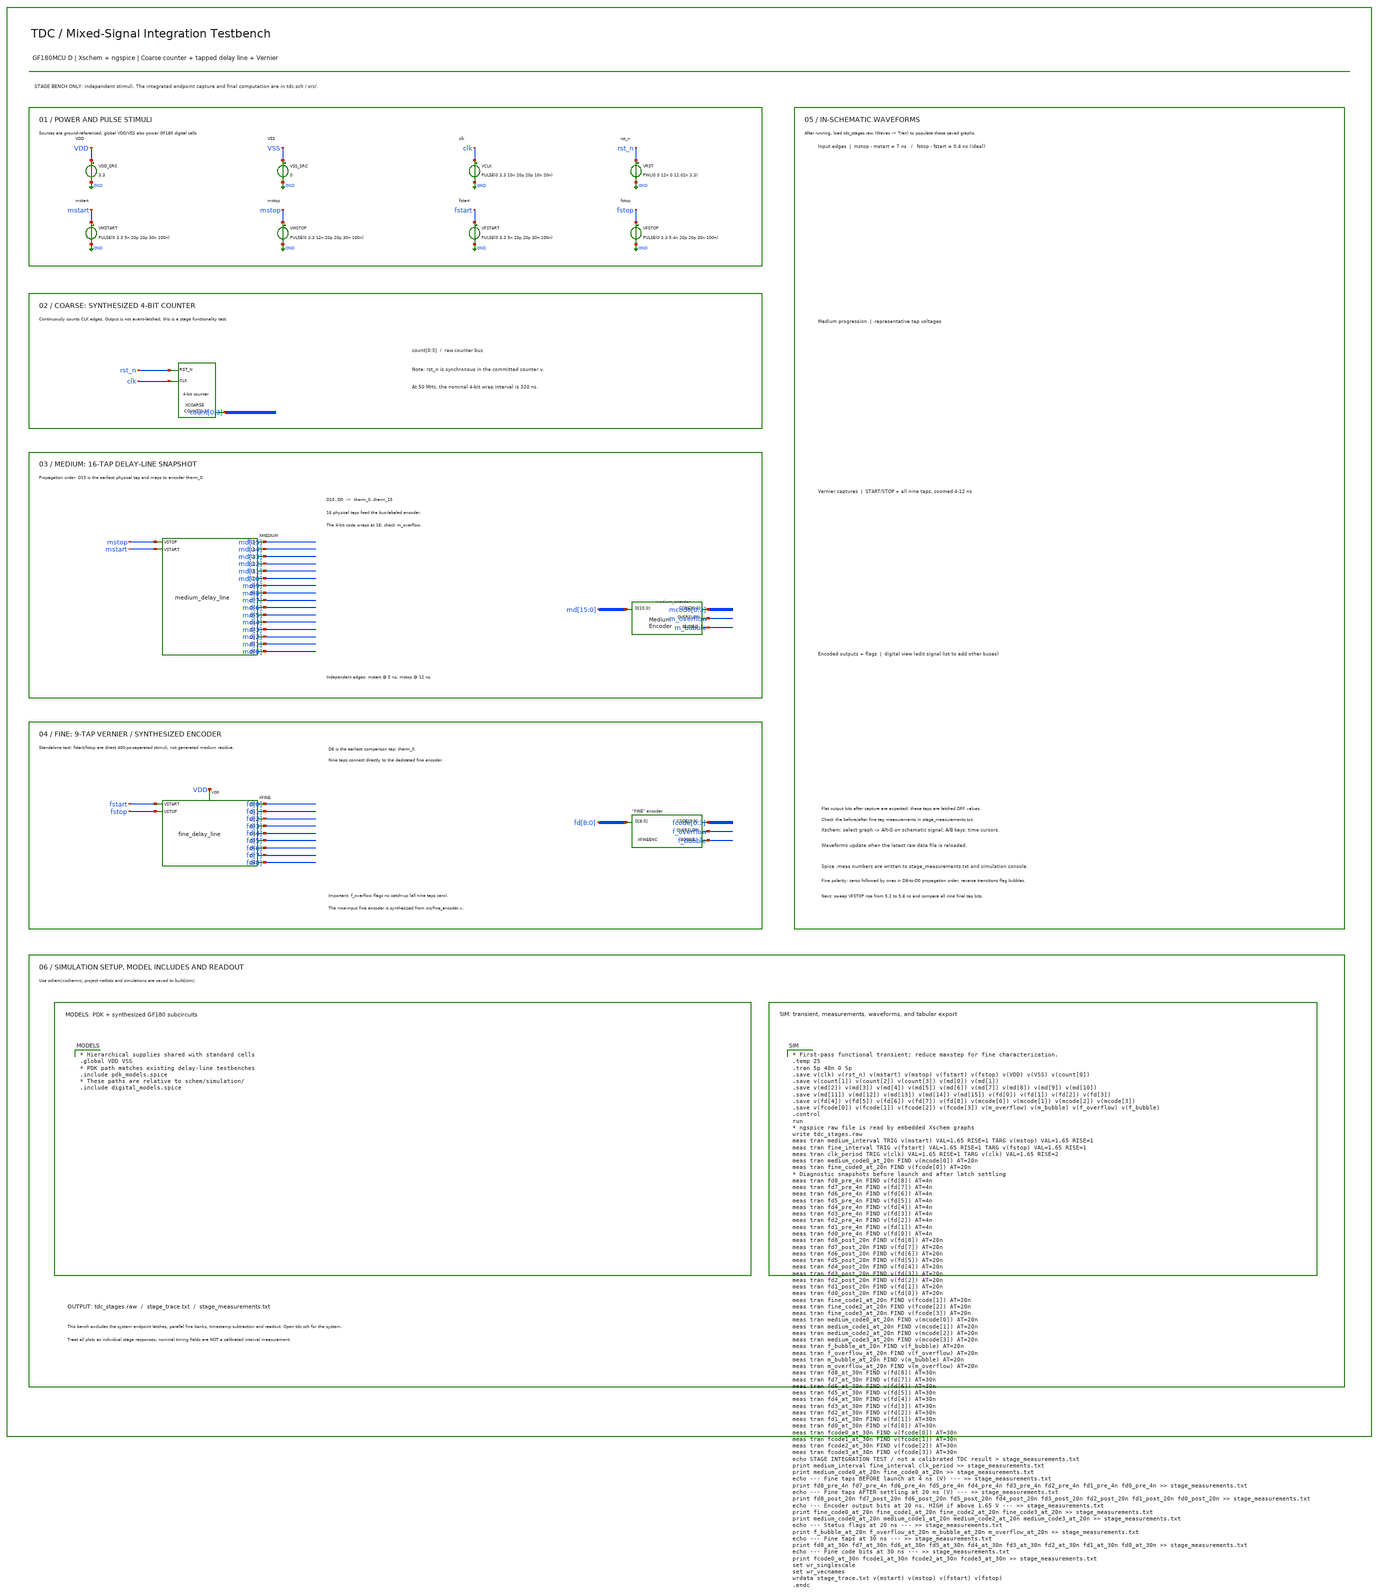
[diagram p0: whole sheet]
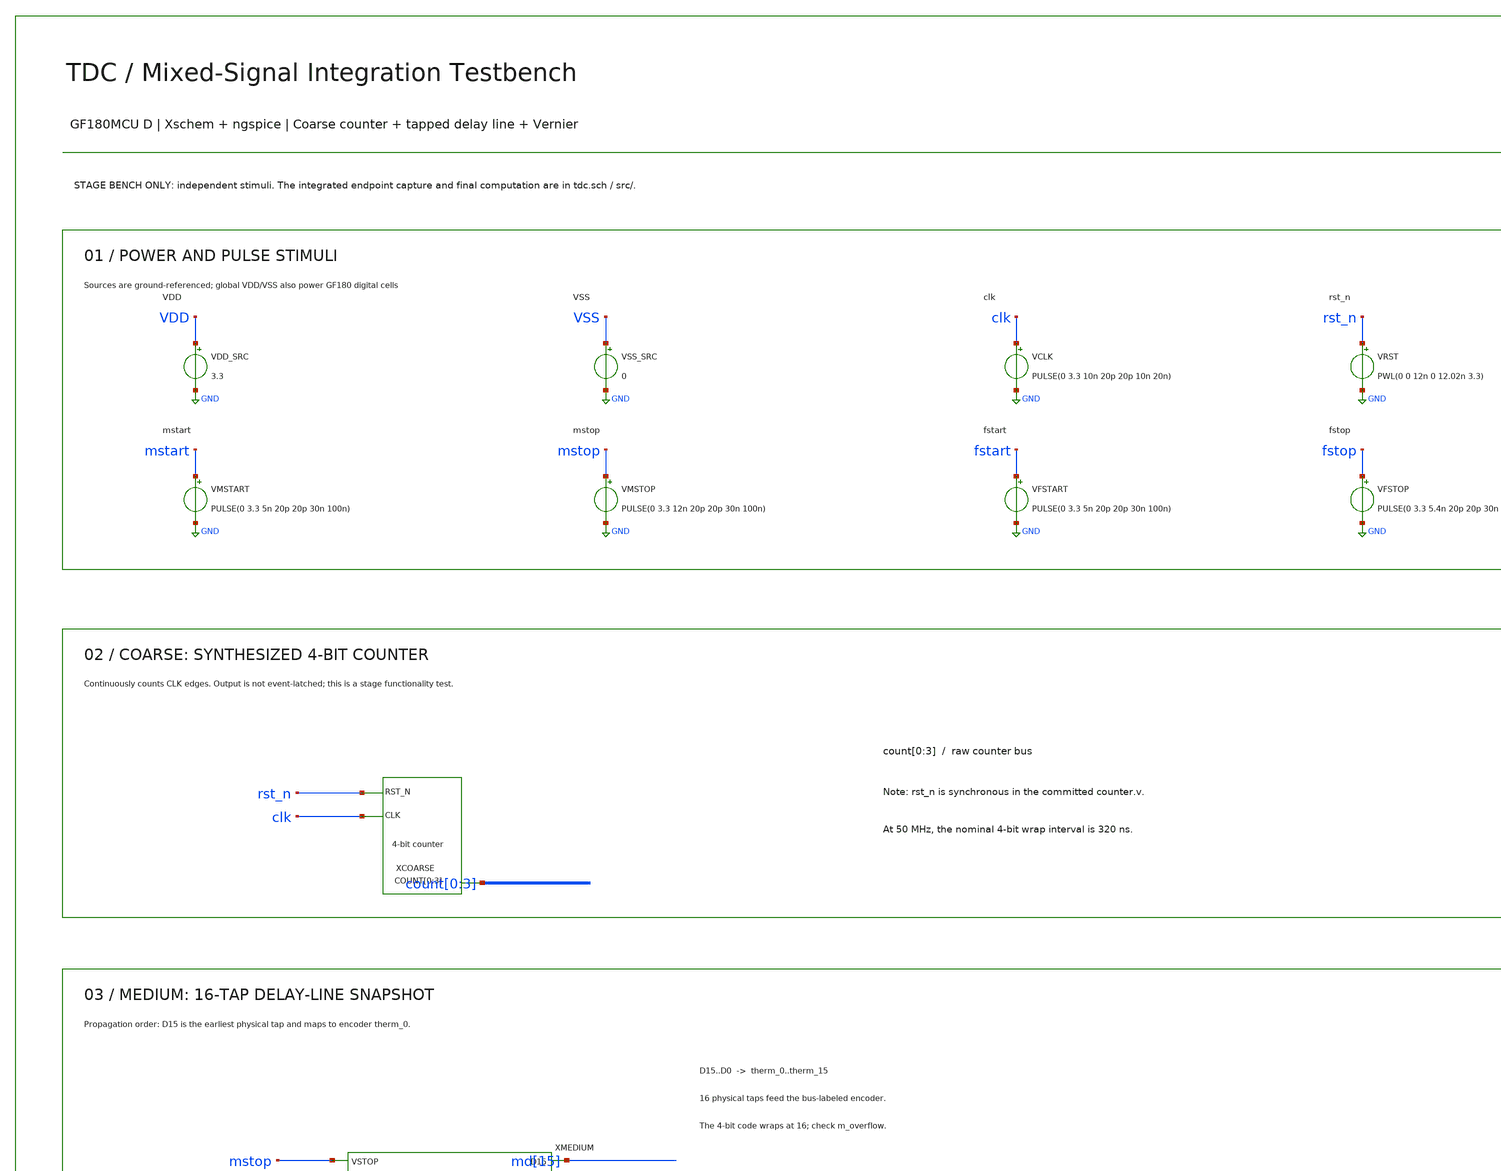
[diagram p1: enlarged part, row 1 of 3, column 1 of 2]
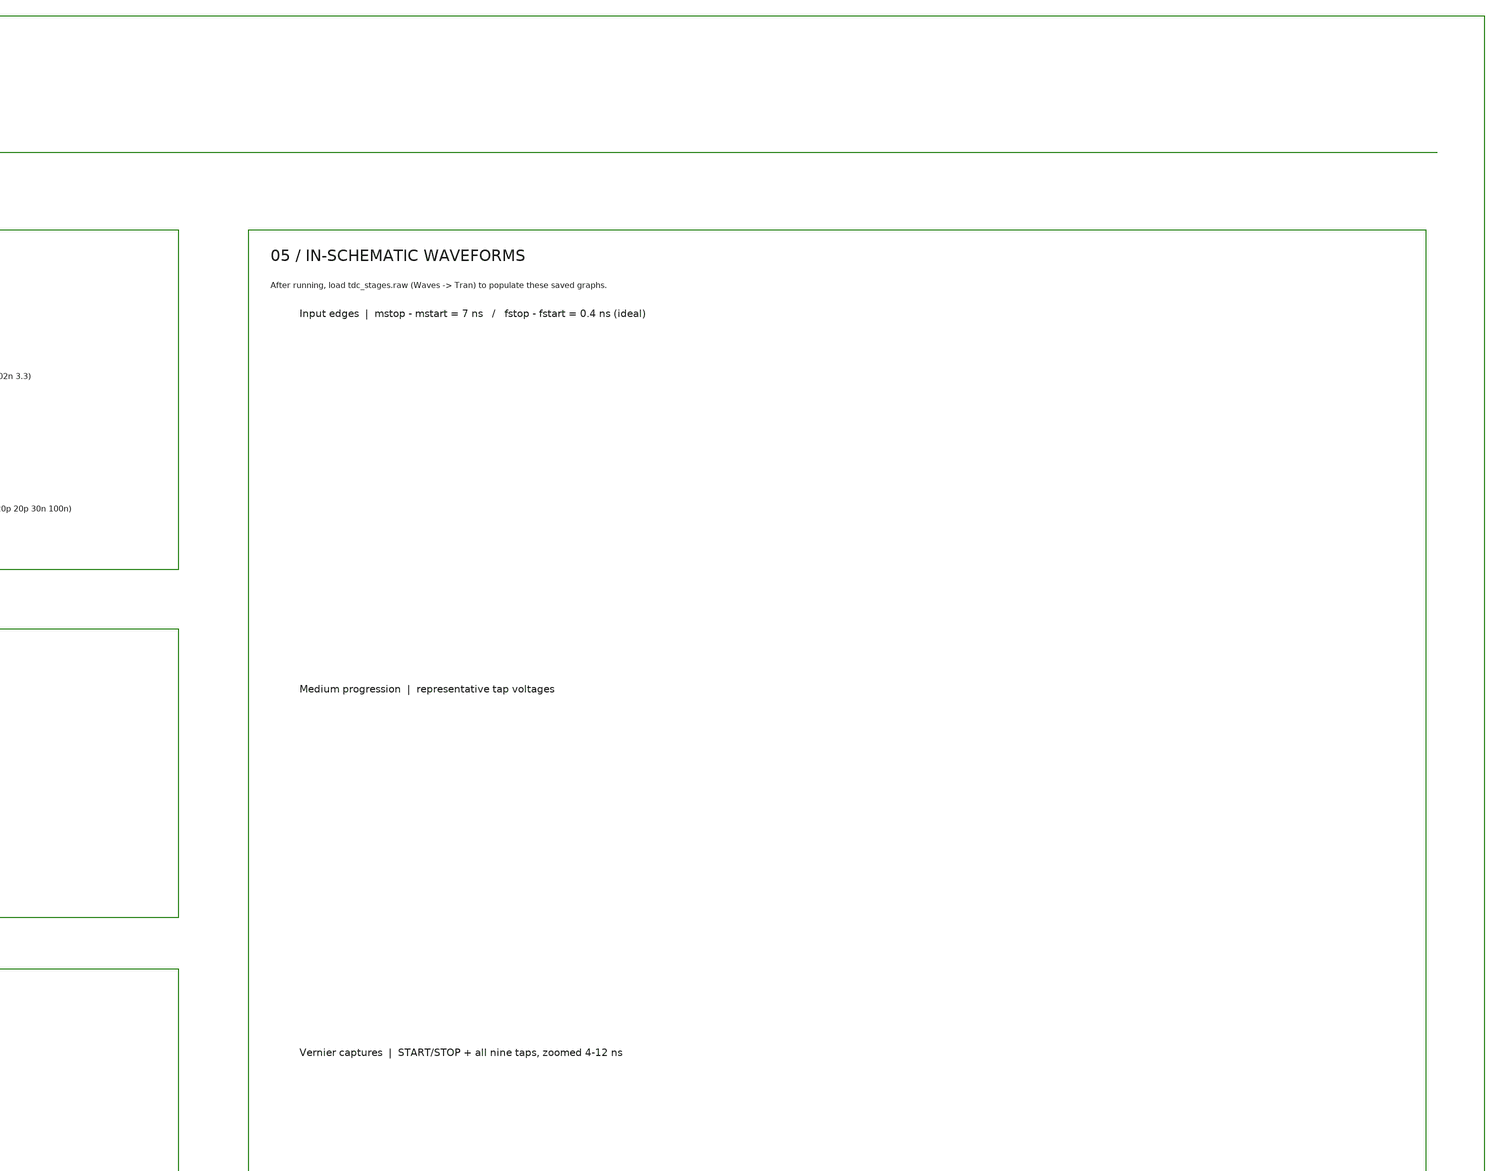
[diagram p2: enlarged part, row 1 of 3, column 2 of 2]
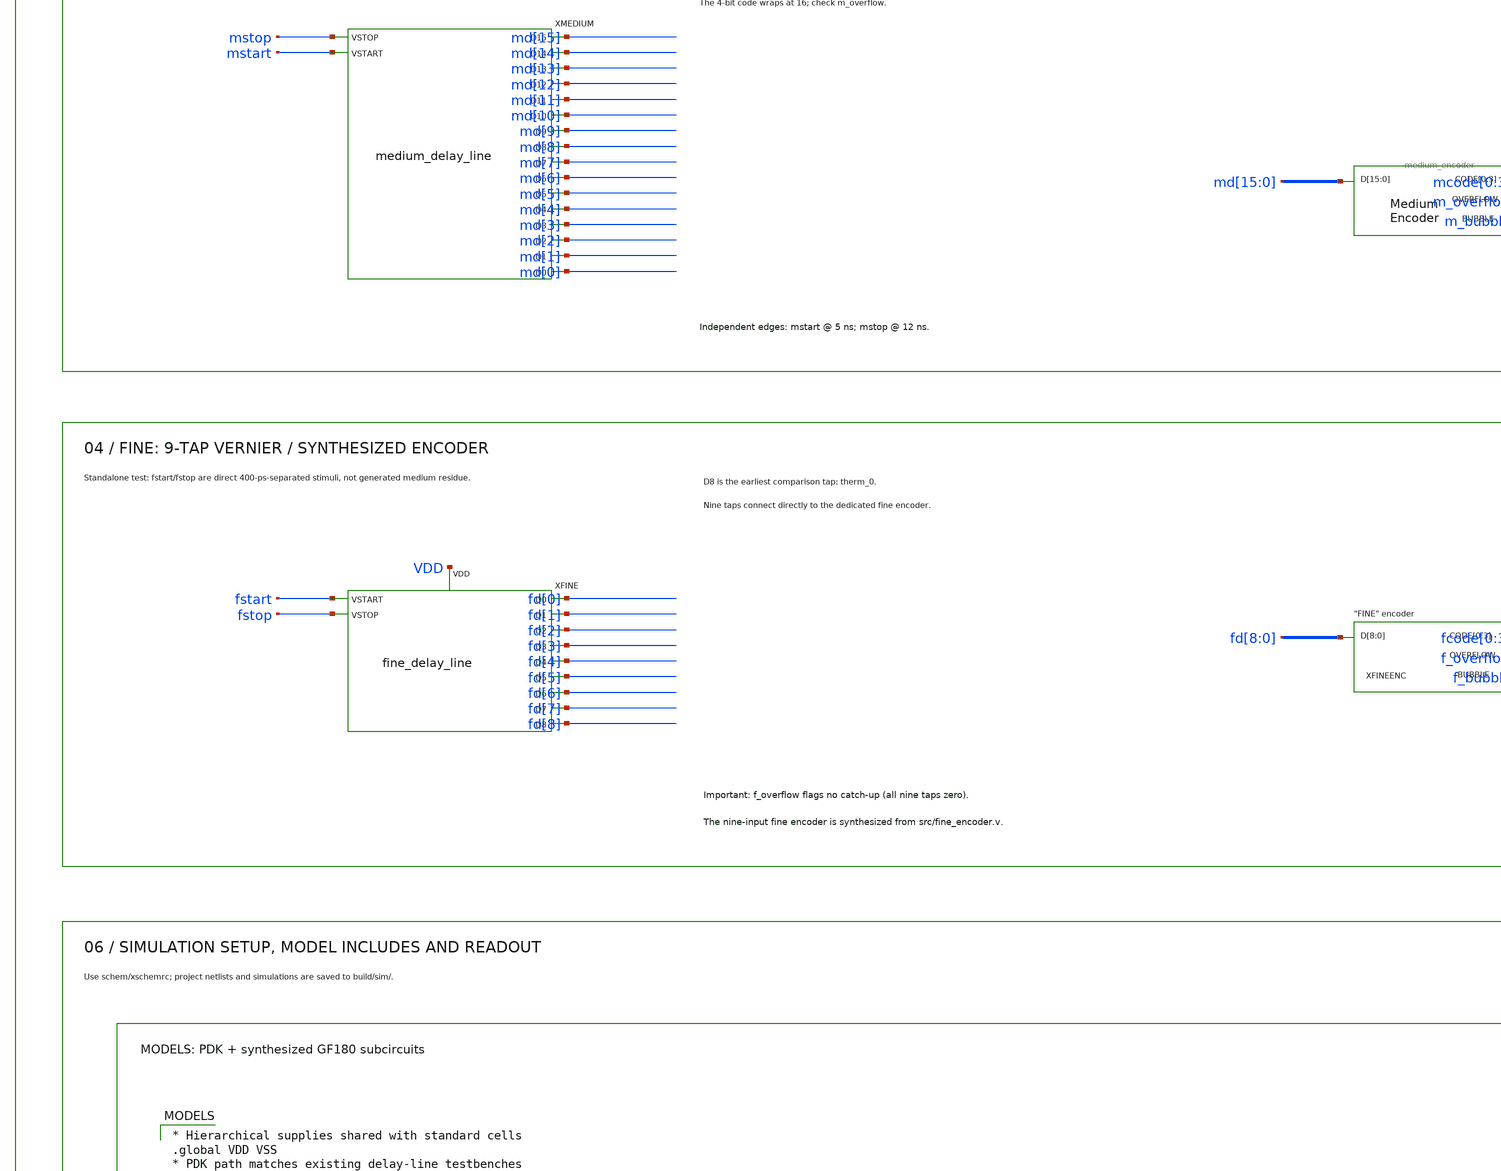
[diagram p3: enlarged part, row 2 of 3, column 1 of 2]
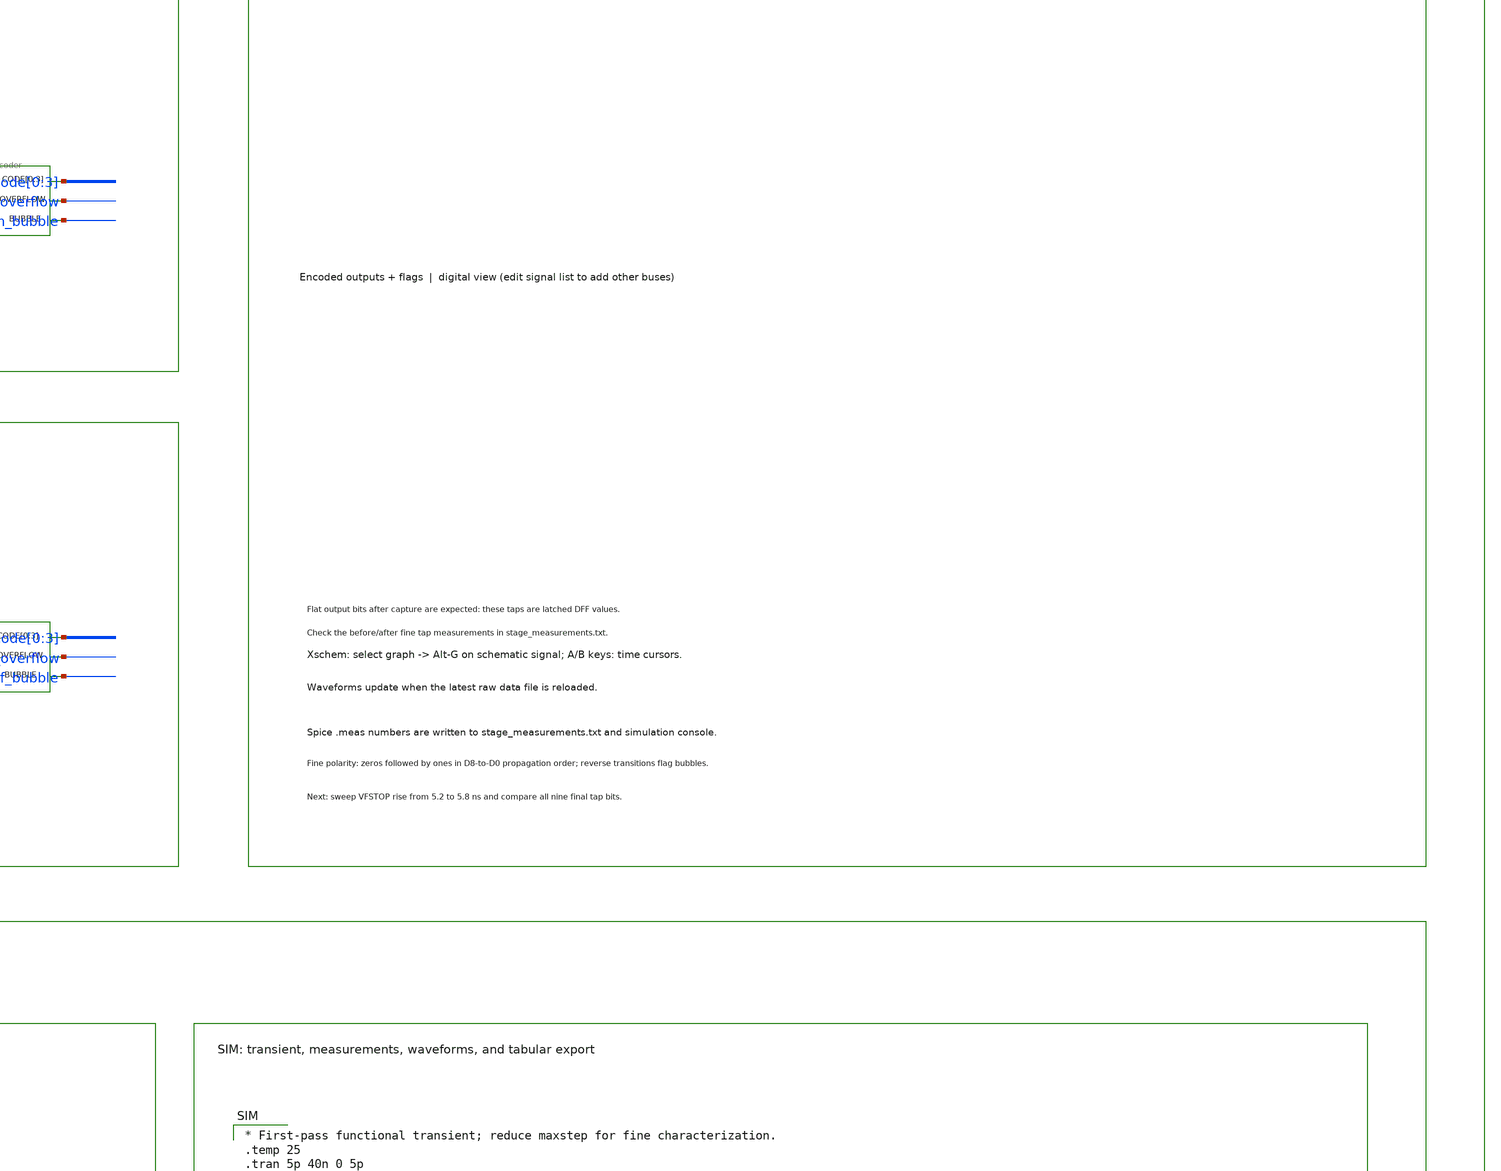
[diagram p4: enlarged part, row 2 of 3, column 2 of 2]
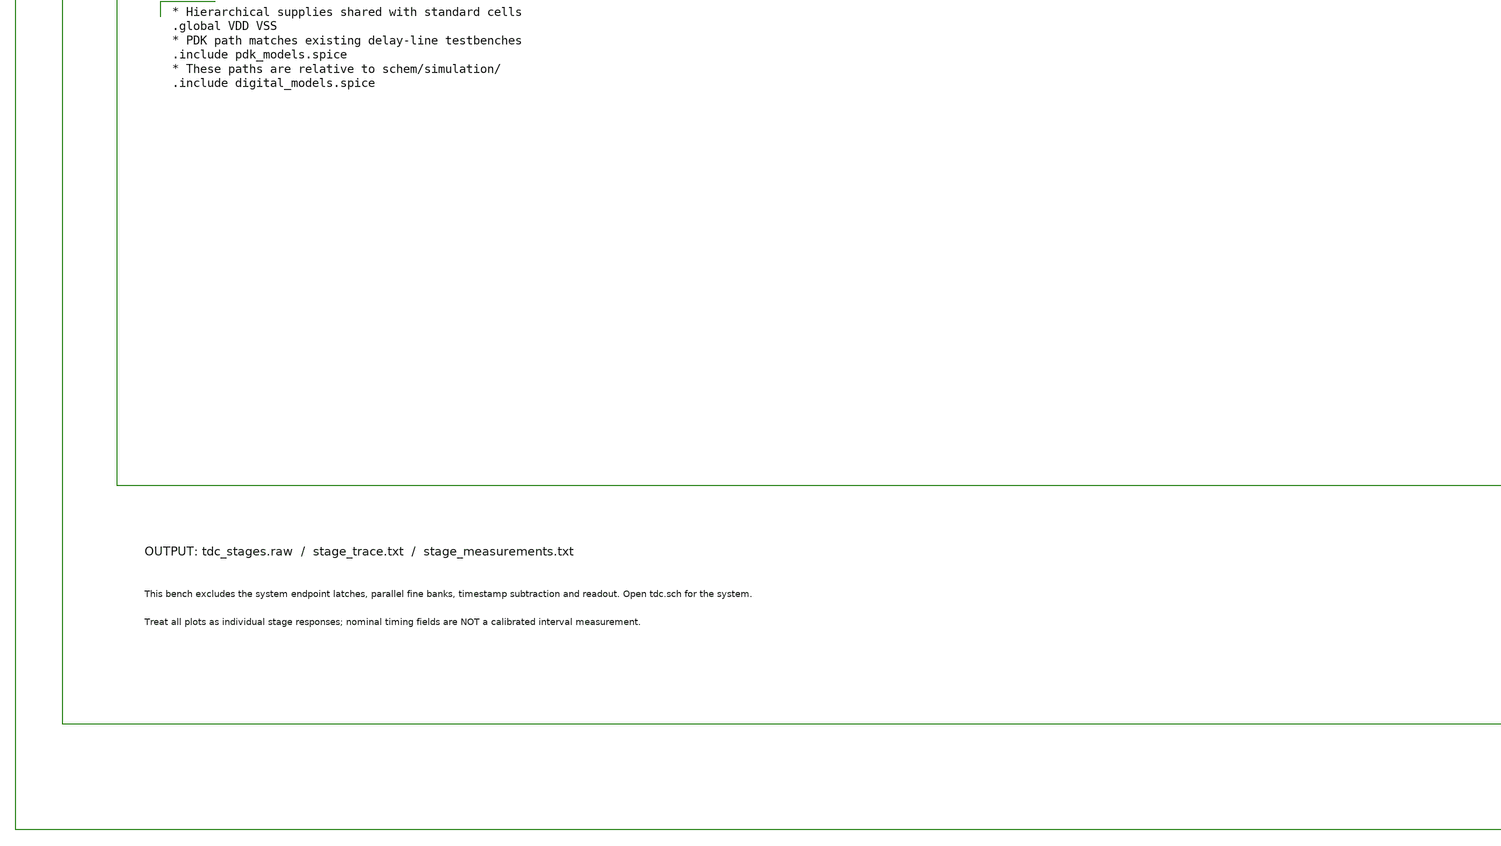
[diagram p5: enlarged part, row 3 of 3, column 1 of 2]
** sch_path: schem/tdc_stages.sch
**.subckt tdc_stages
VDD_SRC VDD GND 3.3
VSS_SRC VSS GND 0
VCLK clk GND PULSE(0 3.3 10n 20p 20p 10n 20n)
VRST rst_n GND PWL(0 0 12n 0 12.02n 3.3)
VMSTART mstart GND PULSE(0 3.3 5n 20p 20p 30n 100n)
VMSTOP mstop GND PULSE(0 3.3 12n 20p 20p 30n 100n)
VFSTART fstart GND PULSE(0 3.3 5n 20p 20p 30n 100n)
VFSTOP fstop GND PULSE(0 3.3 5.4n 20p 20p 30n 100n)
XCOARSE clk rst_n count[0] count[1] count[2] count[3] VDD VSS counter
XMEDIUM mstop md[15] md[2] md[13] md[12] md[11] md[10] md[9] md[8] md[7] md[6] md[5] md[4] md[3]
+ md[14] md[1] md[0] mstart medium_delay_line
XMEDENC md[15] md[14] md[13] md[12] md[11] md[10] md[9] md[8] md[7] md[6] md[5] md[4] md[3] md[2]
+ md[1] md[0] mcode[0] mcode[1] mcode[2] mcode[3] m_overflow m_bubble VDD VSS therm_encoder
XFINE fstart fd[0] fd[5] fd[2] fd[3] fd[4] fd[1] fd[6] fd[7] fd[8] fstop VDD fine_delay_line
XFINEENC fd[8] fd[7] fd[6] fd[5] fd[4] fd[3] fd[2] fd[1] fd[0] fcode[0] fcode[1] fcode[2] fcode[3]
+ f_overflow f_bubble VDD VSS fine_encoder
**** begin user architecture code

* Hierarchical supplies shared with standard cells
.global VDD VSS
* PDK path matches existing delay-line testbenches
.include pdk_models.spice
* These paths are relative to schem/simulation/
.include digital_models.spice


* First-pass functional transient; reduce maxstep for fine characterization.
.temp 25
.tran 5p 40n 0 5p
.save v(clk) v(rst_n) v(mstart) v(mstop) v(fstart) v(fstop) v(VDD) v(VSS) v(count[0])
.save v(count[1]) v(count[2]) v(count[3]) v(md[0]) v(md[1])
.save v(md[2]) v(md[3]) v(md[4]) v(md[5]) v(md[6]) v(md[7]) v(md[8]) v(md[9]) v(md[10])
.save v(md[11]) v(md[12]) v(md[13]) v(md[14]) v(md[15]) v(fd[0]) v(fd[1]) v(fd[2]) v(fd[3])
.save v(fd[4]) v(fd[5]) v(fd[6]) v(fd[7]) v(fd[8]) v(mcode[0]) v(mcode[1]) v(mcode[2]) v(mcode[3])
.save v(fcode[0]) v(fcode[1]) v(fcode[2]) v(fcode[3]) v(m_overflow) v(m_bubble) v(f_overflow) v(f_bubble)
.control
run
* ngspice raw file is read by embedded Xschem graphs
write tdc_stages.raw
meas tran medium_interval TRIG v(mstart) VAL=1.65 RISE=1 TARG v(mstop) VAL=1.65 RISE=1
meas tran fine_interval TRIG v(fstart) VAL=1.65 RISE=1 TARG v(fstop) VAL=1.65 RISE=1
meas tran clk_period TRIG v(clk) VAL=1.65 RISE=1 TARG v(clk) VAL=1.65 RISE=2
meas tran medium_code0_at_20n FIND v(mcode[0]) AT=20n
meas tran fine_code0_at_20n FIND v(fcode[0]) AT=20n
* Diagnostic snapshots before launch and after latch settling
meas tran fd8_pre_4n FIND v(fd[8]) AT=4n
meas tran fd7_pre_4n FIND v(fd[7]) AT=4n
meas tran fd6_pre_4n FIND v(fd[6]) AT=4n
meas tran fd5_pre_4n FIND v(fd[5]) AT=4n
meas tran fd4_pre_4n FIND v(fd[4]) AT=4n
meas tran fd3_pre_4n FIND v(fd[3]) AT=4n
meas tran fd2_pre_4n FIND v(fd[2]) AT=4n
meas tran fd1_pre_4n FIND v(fd[1]) AT=4n
meas tran fd0_pre_4n FIND v(fd[0]) AT=4n
meas tran fd8_post_20n FIND v(fd[8]) AT=20n
meas tran fd7_post_20n FIND v(fd[7]) AT=20n
meas tran fd6_post_20n FIND v(fd[6]) AT=20n
meas tran fd5_post_20n FIND v(fd[5]) AT=20n
meas tran fd4_post_20n FIND v(fd[4]) AT=20n
meas tran fd3_post_20n FIND v(fd[3]) AT=20n
meas tran fd2_post_20n FIND v(fd[2]) AT=20n
meas tran fd1_post_20n FIND v(fd[1]) AT=20n
meas tran fd0_post_20n FIND v(fd[0]) AT=20n
meas tran fine_code1_at_20n FIND v(fcode[1]) AT=20n
meas tran fine_code2_at_20n FIND v(fcode[2]) AT=20n
meas tran fine_code3_at_20n FIND v(fcode[3]) AT=20n
meas tran medium_code0_at_20n FIND v(mcode[0]) AT=20n
meas tran medium_code1_at_20n FIND v(mcode[1]) AT=20n
meas tran medium_code2_at_20n FIND v(mcode[2]) AT=20n
meas tran medium_code3_at_20n FIND v(mcode[3]) AT=20n
meas tran f_bubble_at_20n FIND v(f_bubble) AT=20n
meas tran f_overflow_at_20n FIND v(f_overflow) AT=20n
meas tran m_bubble_at_20n FIND v(m_bubble) AT=20n
meas tran m_overflow_at_20n FIND v(m_overflow) AT=20n
meas tran fd8_at_30n FIND v(fd[8]) AT=30n
meas tran fd7_at_30n FIND v(fd[7]) AT=30n
meas tran fd6_at_30n FIND v(fd[6]) AT=30n
meas tran fd5_at_30n FIND v(fd[5]) AT=30n
meas tran fd4_at_30n FIND v(fd[4]) AT=30n
meas tran fd3_at_30n FIND v(fd[3]) AT=30n
meas tran fd2_at_30n FIND v(fd[2]) AT=30n
meas tran fd1_at_30n FIND v(fd[1]) AT=30n
meas tran fd0_at_30n FIND v(fd[0]) AT=30n
meas tran fcode0_at_30n FIND v(fcode[0]) AT=30n
meas tran fcode1_at_30n FIND v(fcode[1]) AT=30n
meas tran fcode2_at_30n FIND v(fcode[2]) AT=30n
meas tran fcode3_at_30n FIND v(fcode[3]) AT=30n
echo STAGE INTEGRATION TEST / not a calibrated TDC result > stage_measurements.txt
print medium_interval fine_interval clk_period >> stage_measurements.txt
print medium_code0_at_20n fine_code0_at_20n >> stage_measurements.txt
echo --- Fine taps BEFORE launch at 4 ns (V) --- >> stage_measurements.txt
print fd8_pre_4n fd7_pre_4n fd6_pre_4n fd5_pre_4n fd4_pre_4n fd3_pre_4n fd2_pre_4n fd1_pre_4n
+ fd0_pre_4n >> stage_measurements.txt
echo --- Fine taps AFTER settling at 20 ns (V) --- >> stage_measurements.txt
print fd8_post_20n fd7_post_20n fd6_post_20n fd5_post_20n fd4_post_20n fd3_post_20n fd2_post_20n
+ fd1_post_20n fd0_post_20n >> stage_measurements.txt
echo --- Encoder output bits at 20 ns, HIGH if above 1.65 V --- >> stage_measurements.txt
print fine_code0_at_20n fine_code1_at_20n fine_code2_at_20n fine_code3_at_20n >>
+ stage_measurements.txt
print medium_code0_at_20n medium_code1_at_20n medium_code2_at_20n medium_code3_at_20n >>
+ stage_measurements.txt
echo --- Status flags at 20 ns --- >> stage_measurements.txt
print f_bubble_at_20n f_overflow_at_20n m_bubble_at_20n m_overflow_at_20n >> stage_measurements.txt
echo --- Fine taps at 30 ns --- >> stage_measurements.txt
print fd8_at_30n fd7_at_30n fd6_at_30n fd5_at_30n fd4_at_30n fd3_at_30n fd2_at_30n fd1_at_30n
+ fd0_at_30n >> stage_measurements.txt
echo --- Fine code bits at 30 ns --- >> stage_measurements.txt
print fcode0_at_30n fcode1_at_30n fcode2_at_30n fcode3_at_30n >> stage_measurements.txt
set wr_singlescale
set wr_vecnames
wrdata stage_trace.txt v(mstart) v(mstop) v(fstart) v(fstop)
.endc

**** end user architecture code
**.ends
.GLOBAL GND
.end
